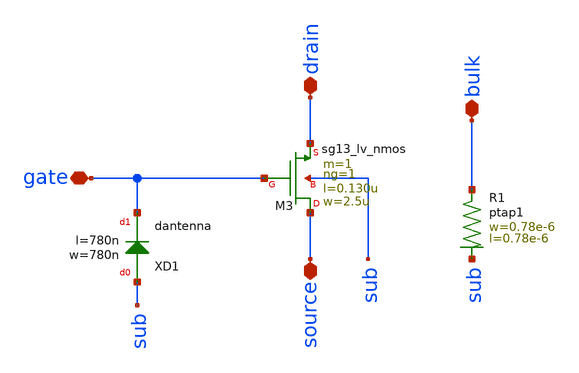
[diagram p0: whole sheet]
** sch_path: ts_pr_May2024/design_data/xschem/nmos1.sch
**.subckt nmos1 drain source bulk gate
*.iopin drain
*.iopin source
*.iopin bulk
*.iopin gate
XR1 bulk sub ptap1 R=262.8 w=0.78e-6 l=0.78e-6
XM3 source gate drain sub sg13_lv_nmos w=2.5u l=0.130u ng=1 m=1 mm_ok=1
XXD1 sub gate dantenna l=780n w=780n
**.ends
.end
